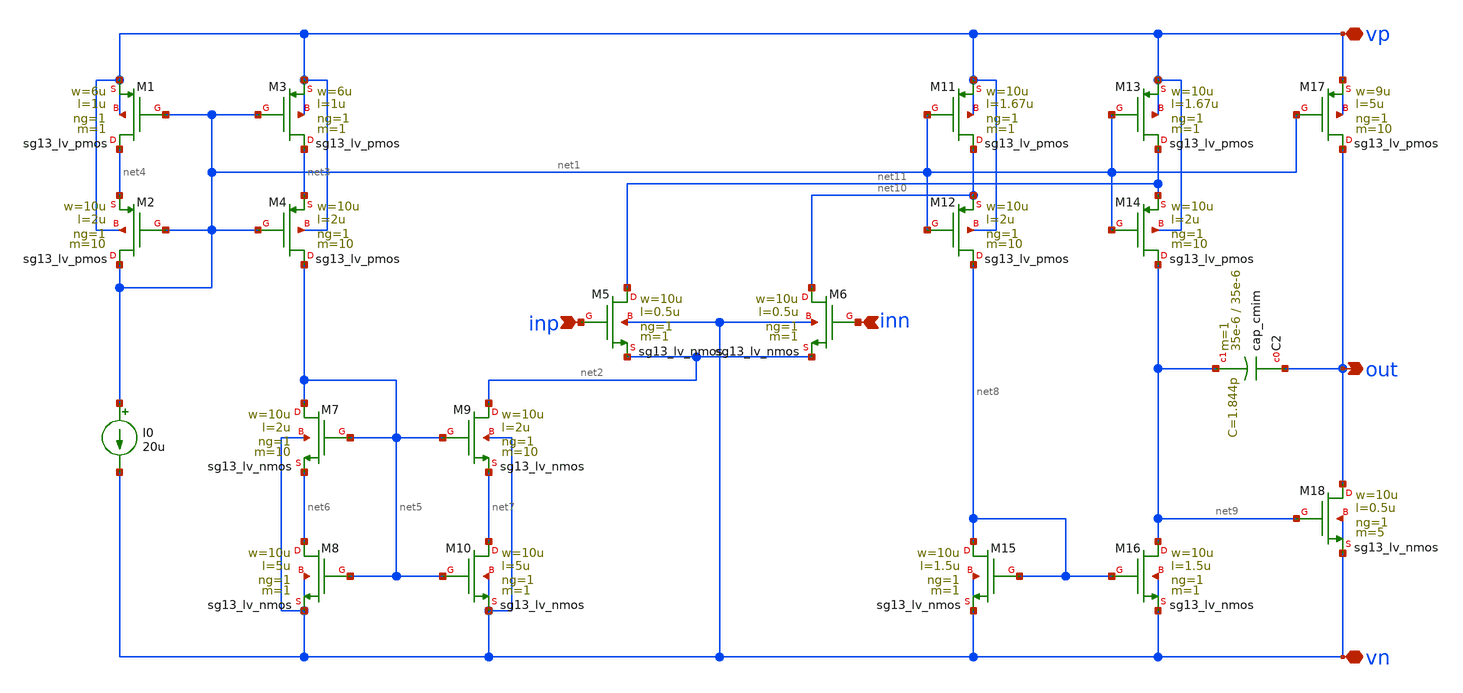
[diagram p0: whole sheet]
** sch_path: TempSensor/design_data/xschem/diff_amp_8-16.sch
**.subckt diff_amp_8-16 inp out inn vn vp
*.ipin inp
*.opin out
*.ipin inn
*.iopin vn
*.iopin vp
XM6 net10 inn net2 vn sg13_lv_nmos w=10u l=0.5u ng=1 m=1 mm_ok=1
XM5 net11 inp net2 vn sg13_lv_nmos w=10u l=0.5u ng=1 m=1 mm_ok=1
XM2 net1 net1 net4 vp sg13_lv_pmos w=10u l=2u ng=1 m=10 mm_ok=1
XM1 net4 net1 vp vp sg13_lv_pmos w=6u l=1u ng=1 m=1 mm_ok=1
XM3 net3 net1 vp vp sg13_lv_pmos w=6u l=1u ng=1 m=1 mm_ok=1
XM4 net5 net1 net3 vp sg13_lv_pmos w=10u l=2u ng=1 m=10 mm_ok=1
XM7 net5 net5 net6 vn sg13_lv_nmos w=10u l=2u ng=1 m=10 mm_ok=1
XM8 net6 net5 vn vn sg13_lv_nmos w=10u l=5u ng=1 m=1 mm_ok=1
XM9 net2 net5 net7 vn sg13_lv_nmos w=10u l=2u ng=1 m=10 mm_ok=1
XM10 net7 net5 vn vn sg13_lv_nmos w=10u l=5u ng=1 m=1 mm_ok=1
XM15 net8 net8 vn vn sg13_lv_nmos w=10u l=1.5u ng=1 m=1 mm_ok=1
XM16 net9 net8 vn vn sg13_lv_nmos w=10u l=1.5u ng=1 m=1 mm_ok=1
XM11 net10 net1 vp vp sg13_lv_pmos w=10u l=1.67u ng=1 m=1 mm_ok=1
XM12 net8 net1 net10 vp sg13_lv_pmos w=10u l=2u ng=1 m=10 mm_ok=1
XM13 net11 net1 vp vp sg13_lv_pmos w=10u l=1.67u ng=1 m=1 mm_ok=1
XM14 net9 net1 net11 vp sg13_lv_pmos w=10u l=2u ng=1 m=10 mm_ok=1
XM17 out net1 vp vp sg13_lv_pmos w=9u l=5u ng=1 m=10 mm_ok=1
XM18 out net9 vn vn sg13_lv_nmos w=10u l=0.5u ng=1 m=5 mm_ok=1
I0 net1 vn 20u
XC2 out net9 cap_cmim w=35e-6 l=35e-6 m=1 mm_ok=1
**.ends
.end
